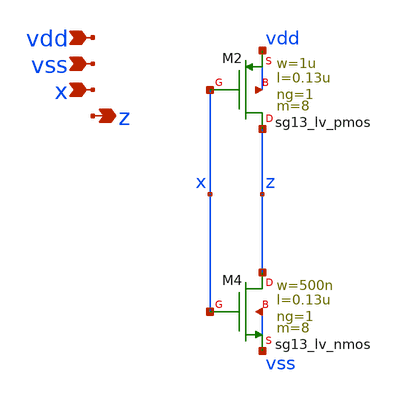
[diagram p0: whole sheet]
** sch_path: MSPHY9932-main/schematic/xschem/buf_8.sch
**.subckt buf_8 vdd vss x z
*.ipin vdd
*.ipin vss
*.ipin x
*.opin z
XM2 z x vdd vdd sg13_lv_pmos w=1u l=0.13u ng=1 m=8 mm_ok=1
XM4 z x vss vss sg13_lv_nmos w=500n l=0.13u ng=1 m=8 mm_ok=1
**.ends
.end
